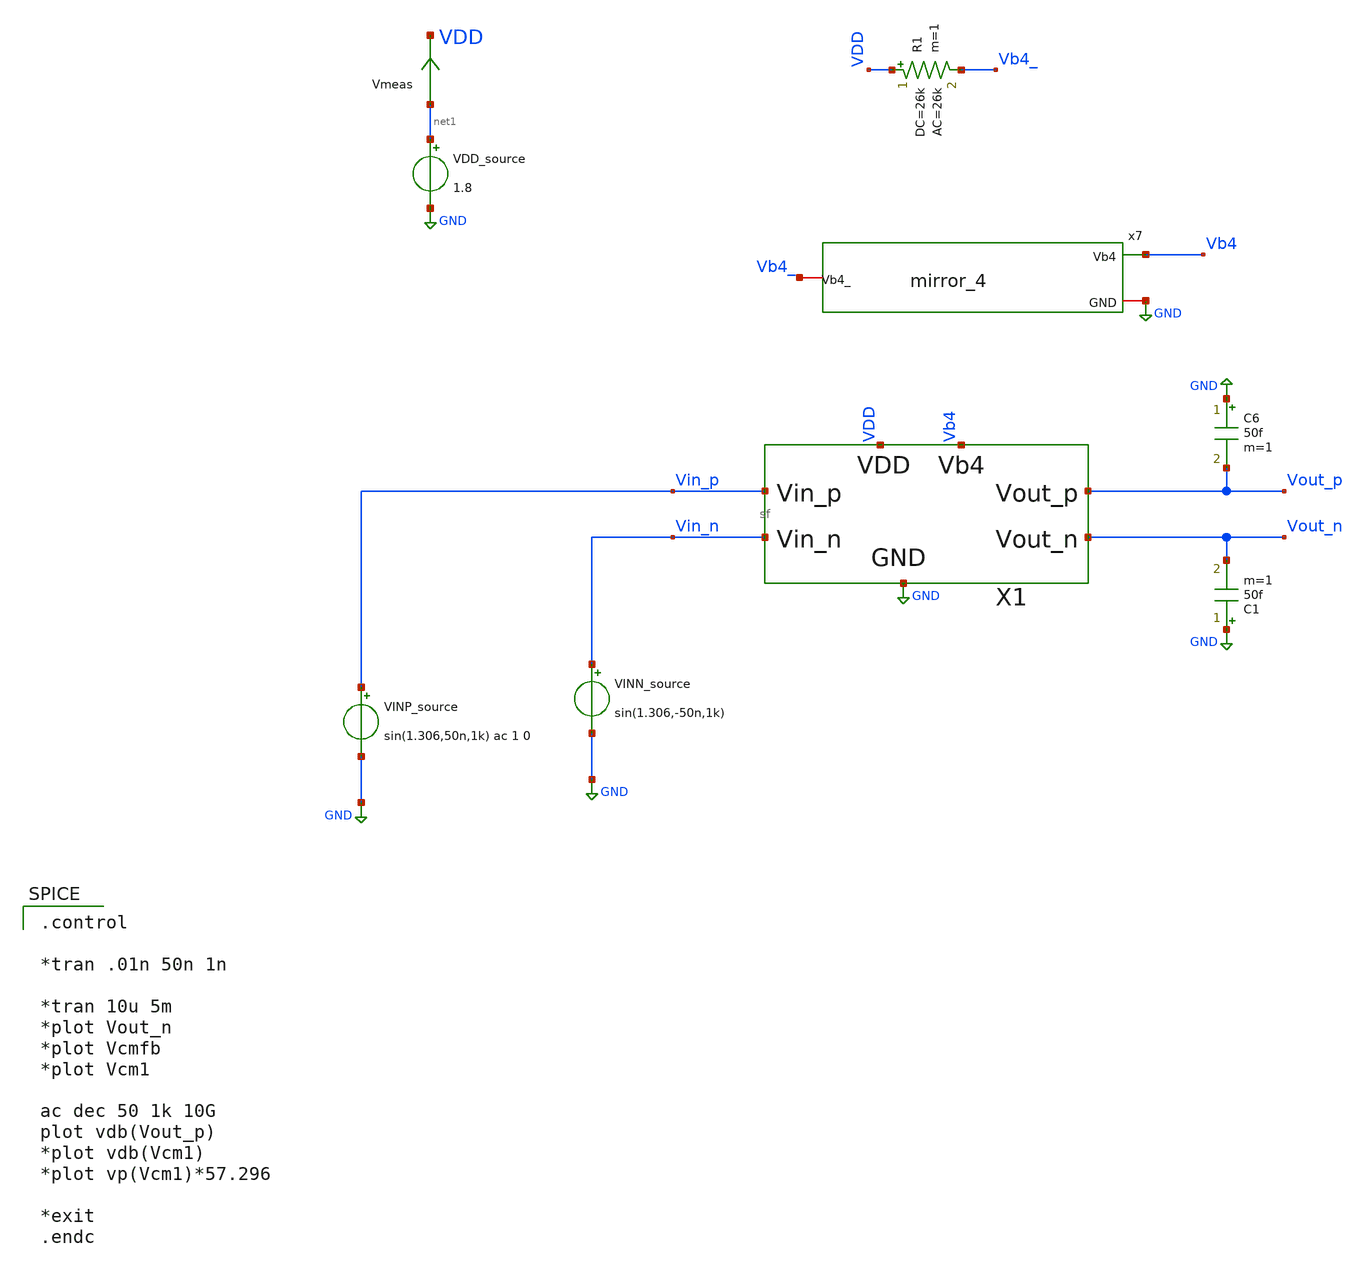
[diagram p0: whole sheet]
** sch_path: xschem/sf_tb.sch
**.subckt sf_tb
VDD_source net1 GND 1.8
Vmeas net1 VDD 0
.save i(vmeas)
C6 GND Vout_p 50f m=1
C1 GND Vout_n 50f m=1
VINP_source Vin_p GND sin(1.306,50n,1k) ac 1 0
VINN_source Vin_n GND sin(1.306,-50n,1k)
X1 VDD GND Vin_p Vin_n Vout_p Vout_n Vb4 sf
R1 VDD Vb4_ 26k ac=26k m=1
x7 Vb4 Vb4_ GND mirror_4
**** begin user architecture code

.include $::SKYWATER_MODELS/cells/nfet_01v8/sky130_fd_pr__nfet_01v8__tt.corner.spice
.include $::SKYWATER_MODELS/cells/pfet_01v8/sky130_fd_pr__pfet_01v8__tt.corner.spice
.include $::SKYWATER_MODELS/cells/nfet_01v8_lvt/sky130_fd_pr__nfet_01v8_lvt__tt.corner.spice
*.include $::SKYWATER_MODELS/cells/nfet_03v3_nvt/sky130_fd_pr__nfet_03v3_nvt__tt.corner.spice
*.include $::SKYWATER_MODELS/cells/nfet_05v0_nvt/sky130_fd_pr__nfet_05v0_nvt__tt.corner.spice
*.include $::SKYWATER_MODELS/cells/esd_nfet_01v8/sky130_fd_pr__esd_nfet_01v8__tt.corner.spice
*.include $::SKYWATER_MODELS/cells/pfet_01v8_lvt/sky130_fd_pr__pfet_01v8_lvt__tt.corner.spice
*.include $::SKYWATER_MODELS/cells/pfet_01v8_hvt/sky130_fd_pr__pfet_01v8_hvt__tt.corner.spice
*.include $::SKYWATER_MODELS/models/corners/tt/nonfet.spice
* Mismatch parameters
.include $::SKYWATER_MODELS/cells/nfet_01v8/sky130_fd_pr__nfet_01v8__mismatch.corner.spice
.include $::SKYWATER_MODELS/cells/pfet_01v8/sky130_fd_pr__pfet_01v8__mismatch.corner.spice
.include $::SKYWATER_MODELS/cells/nfet_01v8_lvt/sky130_fd_pr__nfet_01v8_lvt__mismatch.corner.spice
*.include $::SKYWATER_MODELS/cells/pfet_01v8_lvt/sky130_fd_pr__pfet_01v8_lvt__mismatch.corner.spice
*.include $::SKYWATER_MODELS/cells/pfet_01v8_hvt/sky130_fd_pr__pfet_01v8_hvt__mismatch.corner.spice
*.include $::SKYWATER_MODELS/cells/nfet_g5v0d10v5/sky130_fd_pr__nfet_g5v0d10v5__mismatch.corner.spice
*.include $::SKYWATER_MODELS/cells/pfet_g5v0d10v5/sky130_fd_pr__pfet_g5v0d10v5__mismatch.corner.spice
*.include $::SKYWATER_MODELS/cells/nfet_05v0_nvt/sky130_fd_pr__nfet_05v0_nvt__mismatch.corner.spice
*.include $::SKYWATER_MODELS/cells/nfet_03v3_nvt/sky130_fd_pr__nfet_03v3_nvt__mismatch.corner.spice
* Resistor$::SKYWATER_MODELS/Capacitor
.include $::SKYWATER_MODELS/models/r+c/res_typical__cap_typical.spice
.include $::SKYWATER_MODELS/models/r+c/res_typical__cap_typical__lin.spice
* Special cells
*.include $::SKYWATER_MODELS/models/corners/tt/specialized_cells.spice
* All models
.include $::SKYWATER_MODELS/models/all.spice
* Corner
*.include $::SKYWATER_MODELS/models/corners/tt/rf.spice
.include /home/jared/Documents/GS_Design/tia_post_approval/pex/sf_pex_fixed.spice


.option savecurrents
.control
save all
*NFET

save @m.xm90.msky130_fd_pr__nfet_01v8[vds] @m.xm90.msky130_fd_pr__nfet_01v8[gm]
+ @m.xm90.msky130_fd_pr__nfet_01v8[vth] @m.xm90.msky130_fd_pr__nfet_01v8[vgs] @m.xm90.msky130_fd_pr__nfet_01v8[id]
+ @m.xm90.msky130_fd_pr__nfet_01v8[gds] @m.xm90.msky130_fd_pr__nfet_01v8[cgg] @m.xm90.msky130_fd_pr__nfet_01v8[cgs]
+ @m.xm90.msky130_fd_pr__nfet_01v8[cgd] @m.xm90.msky130_fd_pr__nfet_01v8[cgb] @m.xm90.msky130_fd_pr__nfet_01v8[cdg]
+ @m.xm90.msky130_fd_pr__nfet_01v8[cds] @m.xm90.msky130_fd_pr__nfet_01v8[cdd] @m.xm90.msky130_fd_pr__nfet_01v8[cdb]
+ @m.xm90.msky130_fd_pr__nfet_01v8[csg] @m.xm90.msky130_fd_pr__nfet_01v8[css] @m.xm90.msky130_fd_pr__nfet_01v8[csd]
+ @m.xm90.msky130_fd_pr__nfet_01v8[csb] @m.xm90.msky130_fd_pr__nfet_01v8[cbg] @m.xm90.msky130_fd_pr__nfet_01v8[cbs]
+ @m.xm90.msky130_fd_pr__nfet_01v8[cbd] @m.xm90.msky130_fd_pr__nfet_01v8[cbb]
save @m.xm1.msky130_fd_pr__nfet_01v8[vds] @m.xm1.msky130_fd_pr__nfet_01v8[gm]
+ @m.xm1.msky130_fd_pr__nfet_01v8[vth] @m.xm1.msky130_fd_pr__nfet_01v8[vgs] @m.xm1.msky130_fd_pr__nfet_01v8[id]
+ @m.xm1.msky130_fd_pr__nfet_01v8[gds] @m.xm1.msky130_fd_pr__nfet_01v8[cgg] @m.xm1.msky130_fd_pr__nfet_01v8[cgs]
+ @m.xm1.msky130_fd_pr__nfet_01v8[cgd] @m.xm1.msky130_fd_pr__nfet_01v8[cgb] @m.xm1.msky130_fd_pr__nfet_01v8[cdg]
+ @m.xm1.msky130_fd_pr__nfet_01v8[cds] @m.xm1.msky130_fd_pr__nfet_01v8[cdd] @m.xm1.msky130_fd_pr__nfet_01v8[cdb]
+ @m.xm1.msky130_fd_pr__nfet_01v8[csg] @m.xm1.msky130_fd_pr__nfet_01v8[css] @m.xm1.msky130_fd_pr__nfet_01v8[csd]
+ @m.xm1.msky130_fd_pr__nfet_01v8[csb] @m.xm1.msky130_fd_pr__nfet_01v8[cbg] @m.xm1.msky130_fd_pr__nfet_01v8[cbs]
+ @m.xm1.msky130_fd_pr__nfet_01v8[cbd] @m.xm1.msky130_fd_pr__nfet_01v8[cbb]
save @m.xm2.msky130_fd_pr__nfet_01v8[vds] @m.xm2.msky130_fd_pr__nfet_01v8[gm]
+ @m.xm2.msky130_fd_pr__nfet_01v8[vth] @m.xm2.msky130_fd_pr__nfet_01v8[vgs] @m.xm2.msky130_fd_pr__nfet_01v8[id]
+ @m.xm2.msky130_fd_pr__nfet_01v8[gds] @m.xm2.msky130_fd_pr__nfet_01v8[cgg] @m.xm2.msky130_fd_pr__nfet_01v8[cgs]
+ @m.xm2.msky130_fd_pr__nfet_01v8[cgd] @m.xm2.msky130_fd_pr__nfet_01v8[cgb] @m.xm2.msky130_fd_pr__nfet_01v8[cdg]
+ @m.xm2.msky130_fd_pr__nfet_01v8[cds] @m.xm2.msky130_fd_pr__nfet_01v8[cdd] @m.xm2.msky130_fd_pr__nfet_01v8[cdb]
+ @m.xm2.msky130_fd_pr__nfet_01v8[csg] @m.xm2.msky130_fd_pr__nfet_01v8[css] @m.xm2.msky130_fd_pr__nfet_01v8[csd]
+ @m.xm2.msky130_fd_pr__nfet_01v8[csb] @m.xm2.msky130_fd_pr__nfet_01v8[cbg] @m.xm2.msky130_fd_pr__nfet_01v8[cbs]
+ @m.xm2.msky130_fd_pr__nfet_01v8[cbd] @m.xm2.msky130_fd_pr__nfet_01v8[cbb]
save @m.xm3.msky130_fd_pr__nfet_01v8[vds] @m.xm3.msky130_fd_pr__nfet_01v8[gm]
+ @m.xm3.msky130_fd_pr__nfet_01v8[vth] @m.xm3.msky130_fd_pr__nfet_01v8[vgs] @m.xm3.msky130_fd_pr__nfet_01v8[id]
+ @m.xm3.msky130_fd_pr__nfet_01v8[gds] @m.xm3.msky130_fd_pr__nfet_01v8[cgg] @m.xm3.msky130_fd_pr__nfet_01v8[cgs]
+ @m.xm3.msky130_fd_pr__nfet_01v8[cgd] @m.xm3.msky130_fd_pr__nfet_01v8[cgb] @m.xm3.msky130_fd_pr__nfet_01v8[cdg]
+ @m.xm3.msky130_fd_pr__nfet_01v8[cds] @m.xm3.msky130_fd_pr__nfet_01v8[cdd] @m.xm3.msky130_fd_pr__nfet_01v8[cdb]
+ @m.xm3.msky130_fd_pr__nfet_01v8[csg] @m.xm3.msky130_fd_pr__nfet_01v8[css] @m.xm3.msky130_fd_pr__nfet_01v8[csd]
+ @m.xm3.msky130_fd_pr__nfet_01v8[csb] @m.xm3.msky130_fd_pr__nfet_01v8[cbg] @m.xm3.msky130_fd_pr__nfet_01v8[cbs]
+ @m.xm3.msky130_fd_pr__nfet_01v8[cbd] @m.xm3.msky130_fd_pr__nfet_01v8[cbb]
save @m.xm6.msky130_fd_pr__nfet_01v8[vds] @m.xm6.msky130_fd_pr__nfet_01v8[gm]
+ @m.xm6.msky130_fd_pr__nfet_01v8[vth] @m.xm6.msky130_fd_pr__nfet_01v8[vgs] @m.xm6.msky130_fd_pr__nfet_01v8[id]
+ @m.xm6.msky130_fd_pr__nfet_01v8[gds] @m.xm6.msky130_fd_pr__nfet_01v8[cgg] @m.xm6.msky130_fd_pr__nfet_01v8[cgs]
+ @m.xm6.msky130_fd_pr__nfet_01v8[cgd] @m.xm6.msky130_fd_pr__nfet_01v8[cgb] @m.xm6.msky130_fd_pr__nfet_01v8[cdg]
+ @m.xm6.msky130_fd_pr__nfet_01v8[cds] @m.xm6.msky130_fd_pr__nfet_01v8[cdd] @m.xm6.msky130_fd_pr__nfet_01v8[cdb]
+ @m.xm6.msky130_fd_pr__nfet_01v8[csg] @m.xm6.msky130_fd_pr__nfet_01v8[css] @m.xm6.msky130_fd_pr__nfet_01v8[csd]
+ @m.xm6.msky130_fd_pr__nfet_01v8[csb] @m.xm6.msky130_fd_pr__nfet_01v8[cbg] @m.xm6.msky130_fd_pr__nfet_01v8[cbs]
+ @m.xm6.msky130_fd_pr__nfet_01v8[cbd] @m.xm6.msky130_fd_pr__nfet_01v8[cbb]
save @m.xm7.msky130_fd_pr__nfet_01v8[vds] @m.xm7.msky130_fd_pr__nfet_01v8[gm]
+ @m.xm7.msky130_fd_pr__nfet_01v8[vth] @m.xm7.msky130_fd_pr__nfet_01v8[vgs] @m.xm7.msky130_fd_pr__nfet_01v8[id]
+ @m.xm7.msky130_fd_pr__nfet_01v8[gds] @m.xm7.msky130_fd_pr__nfet_01v8[cgg] @m.xm7.msky130_fd_pr__nfet_01v8[cgs]
+ @m.xm7.msky130_fd_pr__nfet_01v8[cgd] @m.xm7.msky130_fd_pr__nfet_01v8[cgb] @m.xm7.msky130_fd_pr__nfet_01v8[cdg]
+ @m.xm7.msky130_fd_pr__nfet_01v8[cds] @m.xm7.msky130_fd_pr__nfet_01v8[cdd] @m.xm7.msky130_fd_pr__nfet_01v8[cdb]
+ @m.xm7.msky130_fd_pr__nfet_01v8[csg] @m.xm7.msky130_fd_pr__nfet_01v8[css] @m.xm7.msky130_fd_pr__nfet_01v8[csd]
+ @m.xm7.msky130_fd_pr__nfet_01v8[csb] @m.xm7.msky130_fd_pr__nfet_01v8[cbg] @m.xm7.msky130_fd_pr__nfet_01v8[cbs]
+ @m.xm7.msky130_fd_pr__nfet_01v8[cbd] @m.xm7.msky130_fd_pr__nfet_01v8[cbb]
save @m.xm8.msky130_fd_pr__nfet_01v8[vds] @m.xm8.msky130_fd_pr__nfet_01v8[gm]
+ @m.xm8.msky130_fd_pr__nfet_01v8[vth] @m.xm8.msky130_fd_pr__nfet_01v8[vgs] @m.xm8.msky130_fd_pr__nfet_01v8[id]
+ @m.xm8.msky130_fd_pr__nfet_01v8[gds] @m.xm8.msky130_fd_pr__nfet_01v8[cgg] @m.xm8.msky130_fd_pr__nfet_01v8[cgs]
+ @m.xm8.msky130_fd_pr__nfet_01v8[cgd] @m.xm8.msky130_fd_pr__nfet_01v8[cgb] @m.xm8.msky130_fd_pr__nfet_01v8[cdg]
+ @m.xm8.msky130_fd_pr__nfet_01v8[cds] @m.xm8.msky130_fd_pr__nfet_01v8[cdd] @m.xm8.msky130_fd_pr__nfet_01v8[cdb]
+ @m.xm8.msky130_fd_pr__nfet_01v8[csg] @m.xm8.msky130_fd_pr__nfet_01v8[css] @m.xm8.msky130_fd_pr__nfet_01v8[csd]
+ @m.xm8.msky130_fd_pr__nfet_01v8[csb] @m.xm8.msky130_fd_pr__nfet_01v8[cbg] @m.xm8.msky130_fd_pr__nfet_01v8[cbs]
+ @m.xm8.msky130_fd_pr__nfet_01v8[cbd] @m.xm8.msky130_fd_pr__nfet_01v8[cbb]
save @m.xm11.msky130_fd_pr__nfet_01v8[vds] @m.xm11.msky130_fd_pr__nfet_01v8[gm]
+ @m.xm11.msky130_fd_pr__nfet_01v8[vth] @m.xm11.msky130_fd_pr__nfet_01v8[vgs] @m.xm11.msky130_fd_pr__nfet_01v8[id]
+ @m.xm11.msky130_fd_pr__nfet_01v8[gds] @m.xm11.msky130_fd_pr__nfet_01v8[cgg] @m.xm11.msky130_fd_pr__nfet_01v8[cgs]
+ @m.xm11.msky130_fd_pr__nfet_01v8[cgd] @m.xm11.msky130_fd_pr__nfet_01v8[cgb] @m.xm11.msky130_fd_pr__nfet_01v8[cdg]
+ @m.xm11.msky130_fd_pr__nfet_01v8[cds] @m.xm11.msky130_fd_pr__nfet_01v8[cdd] @m.xm11.msky130_fd_pr__nfet_01v8[cdb]
+ @m.xm11.msky130_fd_pr__nfet_01v8[csg] @m.xm11.msky130_fd_pr__nfet_01v8[css] @m.xm11.msky130_fd_pr__nfet_01v8[csd]
+ @m.xm11.msky130_fd_pr__nfet_01v8[csb] @m.xm11.msky130_fd_pr__nfet_01v8[cbg] @m.xm11.msky130_fd_pr__nfet_01v8[cbs]
+ @m.xm11.msky130_fd_pr__nfet_01v8[cbd] @m.xm11.msky130_fd_pr__nfet_01v8[cbb]
save @m.xm12.msky130_fd_pr__nfet_01v8[vds] @m.xm12.msky130_fd_pr__nfet_01v8[gm]
+ @m.xm12.msky130_fd_pr__nfet_01v8[vth] @m.xm12.msky130_fd_pr__nfet_01v8[vgs] @m.xm12.msky130_fd_pr__nfet_01v8[id]
+ @m.xm12.msky130_fd_pr__nfet_01v8[gds] @m.xm12.msky130_fd_pr__nfet_01v8[cgg] @m.xm12.msky130_fd_pr__nfet_01v8[cgs]
+ @m.xm12.msky130_fd_pr__nfet_01v8[cgd] @m.xm12.msky130_fd_pr__nfet_01v8[cgb] @m.xm12.msky130_fd_pr__nfet_01v8[cdg]
+ @m.xm12.msky130_fd_pr__nfet_01v8[cds] @m.xm12.msky130_fd_pr__nfet_01v8[cdd] @m.xm12.msky130_fd_pr__nfet_01v8[cdb]
+ @m.xm12.msky130_fd_pr__nfet_01v8[csg] @m.xm12.msky130_fd_pr__nfet_01v8[css] @m.xm12.msky130_fd_pr__nfet_01v8[csd]
+ @m.xm12.msky130_fd_pr__nfet_01v8[csb] @m.xm12.msky130_fd_pr__nfet_01v8[cbg] @m.xm12.msky130_fd_pr__nfet_01v8[cbs]
+ @m.xm12.msky130_fd_pr__nfet_01v8[cbd] @m.xm12.msky130_fd_pr__nfet_01v8[cbb]
save @m.xm16.msky130_fd_pr__nfet_01v8[vds] @m.xm16.msky130_fd_pr__nfet_01v8[gm]
+ @m.xm16.msky130_fd_pr__nfet_01v8[vth] @m.xm16.msky130_fd_pr__nfet_01v8[vgs] @m.xm16.msky130_fd_pr__nfet_01v8[id]
+ @m.xm16.msky130_fd_pr__nfet_01v8[gds] @m.xm16.msky130_fd_pr__nfet_01v8[cgg] @m.xm16.msky130_fd_pr__nfet_01v8[cgs]
+ @m.xm16.msky130_fd_pr__nfet_01v8[cgd] @m.xm16.msky130_fd_pr__nfet_01v8[cgb] @m.xm16.msky130_fd_pr__nfet_01v8[cdg]
+ @m.xm16.msky130_fd_pr__nfet_01v8[cds] @m.xm16.msky130_fd_pr__nfet_01v8[cdd] @m.xm16.msky130_fd_pr__nfet_01v8[cdb]
+ @m.xm16.msky130_fd_pr__nfet_01v8[csg] @m.xm16.msky130_fd_pr__nfet_01v8[css] @m.xm16.msky130_fd_pr__nfet_01v8[csd]
+ @m.xm16.msky130_fd_pr__nfet_01v8[csb] @m.xm16.msky130_fd_pr__nfet_01v8[cbg] @m.xm16.msky130_fd_pr__nfet_01v8[cbs]
+ @m.xm16.msky130_fd_pr__nfet_01v8[cbd] @m.xm16.msky130_fd_pr__nfet_01v8[cbb]
save @m.xm17.msky130_fd_pr__nfet_01v8_lvt[vds] @m.xm17.msky130_fd_pr__nfet_01v8_lvt[gm]
+ @m.xm17.msky130_fd_pr__nfet_01v8_lvt[vth] @m.xm17.msky130_fd_pr__nfet_01v8_lvt[vgs] @m.xm17.msky130_fd_pr__nfet_01v8_lvt[id]
+ @m.xm17.msky130_fd_pr__nfet_01v8_lvt[gds] @m.xm17.msky130_fd_pr__nfet_01v8_lvt[cgg] @m.xm17.msky130_fd_pr__nfet_01v8_lvt[cgs]
+ @m.xm17.msky130_fd_pr__nfet_01v8_lvt[cgd] @m.xm17.msky130_fd_pr__nfet_01v8_lvt[cgb] @m.xm17.msky130_fd_pr__nfet_01v8_lvt[cdg]
+ @m.xm17.msky130_fd_pr__nfet_01v8_lvt[cds] @m.xm17.msky130_fd_pr__nfet_01v8_lvt[cdd] @m.xm17.msky130_fd_pr__nfet_01v8_lvt[cdb]
+ @m.xm17.msky130_fd_pr__nfet_01v8_lvt[csg] @m.xm17.msky130_fd_pr__nfet_01v8_lvt[css] @m.xm17.msky130_fd_pr__nfet_01v8_lvt[csd]
+ @m.xm17.msky130_fd_pr__nfet_01v8_lvt[csb] @m.xm17.msky130_fd_pr__nfet_01v8_lvt[cbg] @m.xm17.msky130_fd_pr__nfet_01v8_lvt[cbs]
+ @m.xm17.msky130_fd_pr__nfet_01v8_lvt[cbd] @m.xm17.msky130_fd_pr__nfet_01v8_lvt[cbb]
save @m.xm18.msky130_fd_pr__nfet_01v8_lvt[vds] @m.xm18.msky130_fd_pr__nfet_01v8_lvt[gm]
+ @m.xm18.msky130_fd_pr__nfet_01v8_lvt[vth] @m.xm18.msky130_fd_pr__nfet_01v8_lvt[vgs] @m.xm18.msky130_fd_pr__nfet_01v8_lvt[id]
+ @m.xm18.msky130_fd_pr__nfet_01v8_lvt[gds] @m.xm18.msky130_fd_pr__nfet_01v8_lvt[cgg] @m.xm18.msky130_fd_pr__nfet_01v8_lvt[cgs]
+ @m.xm18.msky130_fd_pr__nfet_01v8_lvt[cgd] @m.xm18.msky130_fd_pr__nfet_01v8_lvt[cgb] @m.xm18.msky130_fd_pr__nfet_01v8_lvt[cdg]
+ @m.xm18.msky130_fd_pr__nfet_01v8_lvt[cds] @m.xm18.msky130_fd_pr__nfet_01v8_lvt[cdd] @m.xm18.msky130_fd_pr__nfet_01v8_lvt[cdb]
+ @m.xm18.msky130_fd_pr__nfet_01v8_lvt[csg] @m.xm18.msky130_fd_pr__nfet_01v8_lvt[css] @m.xm18.msky130_fd_pr__nfet_01v8_lvt[csd]
+ @m.xm18.msky130_fd_pr__nfet_01v8_lvt[csb] @m.xm18.msky130_fd_pr__nfet_01v8_lvt[cbg] @m.xm18.msky130_fd_pr__nfet_01v8_lvt[cbs]
+ @m.xm18.msky130_fd_pr__nfet_01v8_lvt[cbd] @m.xm18.msky130_fd_pr__nfet_01v8_lvt[cbb]
save @m.xm19.msky130_fd_pr__nfet_01v8[vds] @m.xm19.msky130_fd_pr__nfet_01v8[gm]
+ @m.xm19.msky130_fd_pr__nfet_01v8[vth] @m.xm19.msky130_fd_pr__nfet_01v8[vgs] @m.xm19.msky130_fd_pr__nfet_01v8[id]
+ @m.xm19.msky130_fd_pr__nfet_01v8[gds] @m.xm19.msky130_fd_pr__nfet_01v8[cgg] @m.xm19.msky130_fd_pr__nfet_01v8[cgs]
+ @m.xm19.msky130_fd_pr__nfet_01v8[cgd] @m.xm19.msky130_fd_pr__nfet_01v8[cgb] @m.xm19.msky130_fd_pr__nfet_01v8[cdg]
+ @m.xm19.msky130_fd_pr__nfet_01v8[cds] @m.xm19.msky130_fd_pr__nfet_01v8[cdd] @m.xm19.msky130_fd_pr__nfet_01v8[cdb]
+ @m.xm19.msky130_fd_pr__nfet_01v8[csg] @m.xm19.msky130_fd_pr__nfet_01v8[css] @m.xm19.msky130_fd_pr__nfet_01v8[csd]
+ @m.xm19.msky130_fd_pr__nfet_01v8[csb] @m.xm19.msky130_fd_pr__nfet_01v8[cbg] @m.xm19.msky130_fd_pr__nfet_01v8[cbs]
+ @m.xm19.msky130_fd_pr__nfet_01v8[cbd] @m.xm19.msky130_fd_pr__nfet_01v8[cbb]
save @m.xm30.msky130_fd_pr__nfet_01v8[vds] @m.xm30.msky130_fd_pr__nfet_01v8[gm]
+ @m.xm30.msky130_fd_pr__nfet_01v8[vth] @m.xm30.msky130_fd_pr__nfet_01v8[vgs] @m.xm30.msky130_fd_pr__nfet_01v8[id]
+ @m.xm30.msky130_fd_pr__nfet_01v8[gds] @m.xm30.msky130_fd_pr__nfet_01v8[cgg] @m.xm30.msky130_fd_pr__nfet_01v8[cgs]
+ @m.xm30.msky130_fd_pr__nfet_01v8[cgd] @m.xm30.msky130_fd_pr__nfet_01v8[cgb] @m.xm30.msky130_fd_pr__nfet_01v8[cdg]
+ @m.xm30.msky130_fd_pr__nfet_01v8[cds] @m.xm30.msky130_fd_pr__nfet_01v8[cdd] @m.xm30.msky130_fd_pr__nfet_01v8[cdb]
+ @m.xm30.msky130_fd_pr__nfet_01v8[csg] @m.xm30.msky130_fd_pr__nfet_01v8[css] @m.xm30.msky130_fd_pr__nfet_01v8[csd]
+ @m.xm30.msky130_fd_pr__nfet_01v8[csb] @m.xm30.msky130_fd_pr__nfet_01v8[cbg] @m.xm30.msky130_fd_pr__nfet_01v8[cbs]
+ @m.xm30.msky130_fd_pr__nfet_01v8[cbd] @m.xm30.msky130_fd_pr__nfet_01v8[cbb]
save @m.xm26.msky130_fd_pr__nfet_01v8[vds] @m.xm26.msky130_fd_pr__nfet_01v8[gm]
+ @m.xm26.msky130_fd_pr__nfet_01v8[vth] @m.xm26.msky130_fd_pr__nfet_01v8[vgs] @m.xm26.msky130_fd_pr__nfet_01v8[id]
+ @m.xm26.msky130_fd_pr__nfet_01v8[gds] @m.xm26.msky130_fd_pr__nfet_01v8[cgg] @m.xm26.msky130_fd_pr__nfet_01v8[cgs]
+ @m.xm26.msky130_fd_pr__nfet_01v8[cgd] @m.xm26.msky130_fd_pr__nfet_01v8[cgb] @m.xm26.msky130_fd_pr__nfet_01v8[cdg]
+ @m.xm26.msky130_fd_pr__nfet_01v8[cds] @m.xm26.msky130_fd_pr__nfet_01v8[cdd] @m.xm26.msky130_fd_pr__nfet_01v8[cdb]
+ @m.xm26.msky130_fd_pr__nfet_01v8[csg] @m.xm26.msky130_fd_pr__nfet_01v8[css] @m.xm26.msky130_fd_pr__nfet_01v8[csd]
+ @m.xm26.msky130_fd_pr__nfet_01v8[csb] @m.xm26.msky130_fd_pr__nfet_01v8[cbg] @m.xm26.msky130_fd_pr__nfet_01v8[cbs]
+ @m.xm26.msky130_fd_pr__nfet_01v8[cbd] @m.xm26.msky130_fd_pr__nfet_01v8[cbb]
save @m.xm27.msky130_fd_pr__nfet_01v8[vds] @m.xm27.msky130_fd_pr__nfet_01v8[gm]
+ @m.xm27.msky130_fd_pr__nfet_01v8[vth] @m.xm27.msky130_fd_pr__nfet_01v8[vgs] @m.xm27.msky130_fd_pr__nfet_01v8[id]
+ @m.xm27.msky130_fd_pr__nfet_01v8[gds] @m.xm27.msky130_fd_pr__nfet_01v8[cgg] @m.xm27.msky130_fd_pr__nfet_01v8[cgs]
+ @m.xm27.msky130_fd_pr__nfet_01v8[cgd] @m.xm27.msky130_fd_pr__nfet_01v8[cgb] @m.xm27.msky130_fd_pr__nfet_01v8[cdg]
+ @m.xm27.msky130_fd_pr__nfet_01v8[cds] @m.xm27.msky130_fd_pr__nfet_01v8[cdd] @m.xm27.msky130_fd_pr__nfet_01v8[cdb]
+ @m.xm27.msky130_fd_pr__nfet_01v8[csg] @m.xm27.msky130_fd_pr__nfet_01v8[css] @m.xm27.msky130_fd_pr__nfet_01v8[csd]
+ @m.xm27.msky130_fd_pr__nfet_01v8[csb] @m.xm27.msky130_fd_pr__nfet_01v8[cbg] @m.xm27.msky130_fd_pr__nfet_01v8[cbs]
+ @m.xm27.msky130_fd_pr__nfet_01v8[cbd] @m.xm27.msky130_fd_pr__nfet_01v8[cbb]

*PFET

save @m.xm91.msky130_fd_pr__pfet_01v8[vds] @m.xm91.msky130_fd_pr__pfet_01v8[gm]
+ @m.xm91.msky130_fd_pr__pfet_01v8[vth] @m.xm91.msky130_fd_pr__pfet_01v8[vgs] @m.xm91.msky130_fd_pr__pfet_01v8[id]
+ @m.xm91.msky130_fd_pr__pfet_01v8[gds] @m.xm91.msky130_fd_pr__pfet_01v8[cgg] @m.xm91.msky130_fd_pr__pfet_01v8[cgs]
+ @m.xm91.msky130_fd_pr__pfet_01v8[cgd] @m.xm91.msky130_fd_pr__pfet_01v8[cgb] @m.xm91.msky130_fd_pr__pfet_01v8[cdg]
+ @m.xm91.msky130_fd_pr__pfet_01v8[cds] @m.xm91.msky130_fd_pr__pfet_01v8[cdd] @m.xm91.msky130_fd_pr__pfet_01v8[cdb]
+ @m.xm91.msky130_fd_pr__pfet_01v8[csg] @m.xm91.msky130_fd_pr__pfet_01v8[css] @m.xm91.msky130_fd_pr__pfet_01v8[csd]
+ @m.xm91.msky130_fd_pr__pfet_01v8[csb] @m.xm91.msky130_fd_pr__pfet_01v8[cbg] @m.xm91.msky130_fd_pr__pfet_01v8[cbs]
+ @m.xm91.msky130_fd_pr__pfet_01v8[cbd] @m.xm91.msky130_fd_pr__pfet_01v8[cbb]
save @m.xm4.msky130_fd_pr__pfet_01v8[vds] @m.xm4.msky130_fd_pr__pfet_01v8[gm]
+ @m.xm4.msky130_fd_pr__pfet_01v8[vth] @m.xm4.msky130_fd_pr__pfet_01v8[vgs] @m.xm4.msky130_fd_pr__pfet_01v8[id]
+ @m.xm4.msky130_fd_pr__pfet_01v8[gds] @m.xm4.msky130_fd_pr__pfet_01v8[cgg] @m.xm4.msky130_fd_pr__pfet_01v8[cgs]
+ @m.xm4.msky130_fd_pr__pfet_01v8[cgd] @m.xm4.msky130_fd_pr__pfet_01v8[cgb] @m.xm4.msky130_fd_pr__pfet_01v8[cdg]
+ @m.xm4.msky130_fd_pr__pfet_01v8[cds] @m.xm4.msky130_fd_pr__pfet_01v8[cdd] @m.xm4.msky130_fd_pr__pfet_01v8[cdb]
+ @m.xm4.msky130_fd_pr__pfet_01v8[csg] @m.xm4.msky130_fd_pr__pfet_01v8[css] @m.xm4.msky130_fd_pr__pfet_01v8[csd]
+ @m.xm4.msky130_fd_pr__pfet_01v8[csb] @m.xm4.msky130_fd_pr__pfet_01v8[cbg] @m.xm4.msky130_fd_pr__pfet_01v8[cbs]
+ @m.xm4.msky130_fd_pr__pfet_01v8[cbd] @m.xm4.msky130_fd_pr__pfet_01v8[cbb]
save @m.xm5.msky130_fd_pr__pfet_01v8[vds] @m.xm5.msky130_fd_pr__pfet_01v8[gm]
+ @m.xm5.msky130_fd_pr__pfet_01v8[vth] @m.xm5.msky130_fd_pr__pfet_01v8[vgs] @m.xm5.msky130_fd_pr__pfet_01v8[id]
+ @m.xm5.msky130_fd_pr__pfet_01v8[gds] @m.xm5.msky130_fd_pr__pfet_01v8[cgg] @m.xm5.msky130_fd_pr__pfet_01v8[cgs]
+ @m.xm5.msky130_fd_pr__pfet_01v8[cgd] @m.xm5.msky130_fd_pr__pfet_01v8[cgb] @m.xm5.msky130_fd_pr__pfet_01v8[cdg]
+ @m.xm5.msky130_fd_pr__pfet_01v8[cds] @m.xm5.msky130_fd_pr__pfet_01v8[cdd] @m.xm5.msky130_fd_pr__pfet_01v8[cdb]
+ @m.xm5.msky130_fd_pr__pfet_01v8[csg] @m.xm5.msky130_fd_pr__pfet_01v8[css] @m.xm5.msky130_fd_pr__pfet_01v8[csd]
+ @m.xm5.msky130_fd_pr__pfet_01v8[csb] @m.xm5.msky130_fd_pr__pfet_01v8[cbg] @m.xm5.msky130_fd_pr__pfet_01v8[cbs]
+ @m.xm5.msky130_fd_pr__pfet_01v8[cbd] @m.xm5.msky130_fd_pr__pfet_01v8[cbb]
save @m.xm9.msky130_fd_pr__pfet_01v8[vds] @m.xm9.msky130_fd_pr__pfet_01v8[gm]
+ @m.xm9.msky130_fd_pr__pfet_01v8[vth] @m.xm9.msky130_fd_pr__pfet_01v8[vgs] @m.xm9.msky130_fd_pr__pfet_01v8[id]
+ @m.xm9.msky130_fd_pr__pfet_01v8[gds] @m.xm9.msky130_fd_pr__pfet_01v8[cgg] @m.xm9.msky130_fd_pr__pfet_01v8[cgs]
+ @m.xm9.msky130_fd_pr__pfet_01v8[cgd] @m.xm9.msky130_fd_pr__pfet_01v8[cgb] @m.xm9.msky130_fd_pr__pfet_01v8[cdg]
+ @m.xm9.msky130_fd_pr__pfet_01v8[cds] @m.xm9.msky130_fd_pr__pfet_01v8[cdd] @m.xm9.msky130_fd_pr__pfet_01v8[cdb]
+ @m.xm9.msky130_fd_pr__pfet_01v8[csg] @m.xm9.msky130_fd_pr__pfet_01v8[css] @m.xm9.msky130_fd_pr__pfet_01v8[csd]
+ @m.xm9.msky130_fd_pr__pfet_01v8[csb] @m.xm9.msky130_fd_pr__pfet_01v8[cbg] @m.xm9.msky130_fd_pr__pfet_01v8[cbs]
+ @m.xm9.msky130_fd_pr__pfet_01v8[cbd] @m.xm9.msky130_fd_pr__pfet_01v8[cbb]
save @m.xm10.msky130_fd_pr__pfet_01v8[vds] @m.xm10.msky130_fd_pr__pfet_01v8[gm]
+ @m.xm10.msky130_fd_pr__pfet_01v8[vth] @m.xm10.msky130_fd_pr__pfet_01v8[vgs] @m.xm10.msky130_fd_pr__pfet_01v8[id]
+ @m.xm10.msky130_fd_pr__pfet_01v8[gds] @m.xm10.msky130_fd_pr__pfet_01v8[cgg] @m.xm10.msky130_fd_pr__pfet_01v8[cgs]
+ @m.xm10.msky130_fd_pr__pfet_01v8[cgd] @m.xm10.msky130_fd_pr__pfet_01v8[cgb] @m.xm10.msky130_fd_pr__pfet_01v8[cdg]
+ @m.xm10.msky130_fd_pr__pfet_01v8[cds] @m.xm10.msky130_fd_pr__pfet_01v8[cdd] @m.xm10.msky130_fd_pr__pfet_01v8[cdb]
+ @m.xm10.msky130_fd_pr__pfet_01v8[csg] @m.xm10.msky130_fd_pr__pfet_01v8[css] @m.xm10.msky130_fd_pr__pfet_01v8[csd]
+ @m.xm10.msky130_fd_pr__pfet_01v8[csb] @m.xm10.msky130_fd_pr__pfet_01v8[cbg] @m.xm10.msky130_fd_pr__pfet_01v8[cbs]
+ @m.xm10.msky130_fd_pr__pfet_01v8[cbd] @m.xm10.msky130_fd_pr__pfet_01v8[cbb]
save @m.xm13.msky130_fd_pr__pfet_01v8[vds] @m.xm13.msky130_fd_pr__pfet_01v8[gm]
+ @m.xm13.msky130_fd_pr__pfet_01v8[vth] @m.xm13.msky130_fd_pr__pfet_01v8[vgs] @m.xm13.msky130_fd_pr__pfet_01v8[id]
+ @m.xm13.msky130_fd_pr__pfet_01v8[gds] @m.xm13.msky130_fd_pr__pfet_01v8[cgg] @m.xm13.msky130_fd_pr__pfet_01v8[cgs]
+ @m.xm13.msky130_fd_pr__pfet_01v8[cgd] @m.xm13.msky130_fd_pr__pfet_01v8[cgb] @m.xm13.msky130_fd_pr__pfet_01v8[cdg]
+ @m.xm13.msky130_fd_pr__pfet_01v8[cds] @m.xm13.msky130_fd_pr__pfet_01v8[cdd] @m.xm13.msky130_fd_pr__pfet_01v8[cdb]
+ @m.xm13.msky130_fd_pr__pfet_01v8[csg] @m.xm13.msky130_fd_pr__pfet_01v8[css] @m.xm13.msky130_fd_pr__pfet_01v8[csd]
+ @m.xm13.msky130_fd_pr__pfet_01v8[csb] @m.xm13.msky130_fd_pr__pfet_01v8[cbg] @m.xm13.msky130_fd_pr__pfet_01v8[cbs]
+ @m.xm13.msky130_fd_pr__pfet_01v8[cbd] @m.xm13.msky130_fd_pr__pfet_01v8[cbb]
save @m.xm14.msky130_fd_pr__pfet_01v8[vds] @m.xm14.msky130_fd_pr__pfet_01v8[gm]
+ @m.xm14.msky130_fd_pr__pfet_01v8[vth] @m.xm14.msky130_fd_pr__pfet_01v8[vgs] @m.xm14.msky130_fd_pr__pfet_01v8[id]
+ @m.xm14.msky130_fd_pr__pfet_01v8[gds] @m.xm14.msky130_fd_pr__pfet_01v8[cgg] @m.xm14.msky130_fd_pr__pfet_01v8[cgs]
+ @m.xm14.msky130_fd_pr__pfet_01v8[cgd] @m.xm14.msky130_fd_pr__pfet_01v8[cgb] @m.xm14.msky130_fd_pr__pfet_01v8[cdg]
+ @m.xm14.msky130_fd_pr__pfet_01v8[cds] @m.xm14.msky130_fd_pr__pfet_01v8[cdd] @m.xm14.msky130_fd_pr__pfet_01v8[cdb]
+ @m.xm14.msky130_fd_pr__pfet_01v8[csg] @m.xm14.msky130_fd_pr__pfet_01v8[css] @m.xm14.msky130_fd_pr__pfet_01v8[csd]
+ @m.xm14.msky130_fd_pr__pfet_01v8[csb] @m.xm14.msky130_fd_pr__pfet_01v8[cbg] @m.xm14.msky130_fd_pr__pfet_01v8[cbs]
+ @m.xm14.msky130_fd_pr__pfet_01v8[cbd] @m.xm14.msky130_fd_pr__pfet_01v8[cbb]
save @m.xm24.msky130_fd_pr__pfet_01v8[vds] @m.xm24.msky130_fd_pr__pfet_01v8[gm]
+ @m.xm24.msky130_fd_pr__pfet_01v8[vth] @m.xm24.msky130_fd_pr__pfet_01v8[vgs] @m.xm24.msky130_fd_pr__pfet_01v8[id]
+ @m.xm24.msky130_fd_pr__pfet_01v8[gds] @m.xm24.msky130_fd_pr__pfet_01v8[cgg] @m.xm24.msky130_fd_pr__pfet_01v8[cgs]
+ @m.xm24.msky130_fd_pr__pfet_01v8[cgd] @m.xm24.msky130_fd_pr__pfet_01v8[cgb] @m.xm24.msky130_fd_pr__pfet_01v8[cdg]
+ @m.xm24.msky130_fd_pr__pfet_01v8[cds] @m.xm24.msky130_fd_pr__pfet_01v8[cdd] @m.xm24.msky130_fd_pr__pfet_01v8[cdb]
+ @m.xm24.msky130_fd_pr__pfet_01v8[csg] @m.xm24.msky130_fd_pr__pfet_01v8[css] @m.xm24.msky130_fd_pr__pfet_01v8[csd]
+ @m.xm24.msky130_fd_pr__pfet_01v8[csb] @m.xm24.msky130_fd_pr__pfet_01v8[cbg] @m.xm24.msky130_fd_pr__pfet_01v8[cbs]
+ @m.xm24.msky130_fd_pr__pfet_01v8[cbd] @m.xm24.msky130_fd_pr__pfet_01v8[cbb]
save @m.xm25.msky130_fd_pr__pfet_01v8[vds] @m.xm25.msky130_fd_pr__pfet_01v8[gm]
+ @m.xm25.msky130_fd_pr__pfet_01v8[vth] @m.xm25.msky130_fd_pr__pfet_01v8[vgs] @m.xm25.msky130_fd_pr__pfet_01v8[id]
+ @m.xm25.msky130_fd_pr__pfet_01v8[gds] @m.xm25.msky130_fd_pr__pfet_01v8[cgg] @m.xm25.msky130_fd_pr__pfet_01v8[cgs]
+ @m.xm25.msky130_fd_pr__pfet_01v8[cgd] @m.xm25.msky130_fd_pr__pfet_01v8[cgb] @m.xm25.msky130_fd_pr__pfet_01v8[cdg]
+ @m.xm25.msky130_fd_pr__pfet_01v8[cds] @m.xm25.msky130_fd_pr__pfet_01v8[cdd] @m.xm25.msky130_fd_pr__pfet_01v8[cdb]
+ @m.xm25.msky130_fd_pr__pfet_01v8[csg] @m.xm25.msky130_fd_pr__pfet_01v8[css] @m.xm25.msky130_fd_pr__pfet_01v8[csd]
+ @m.xm25.msky130_fd_pr__pfet_01v8[csb] @m.xm25.msky130_fd_pr__pfet_01v8[cbg] @m.xm25.msky130_fd_pr__pfet_01v8[cbs]
+ @m.xm25.msky130_fd_pr__pfet_01v8[cbd] @m.xm25.msky130_fd_pr__pfet_01v8[cbb]

op
write sf_tb.raw
.endc


.control

*tran .01n 50n 1n

*tran 10u 5m
*plot Vout_n
*plot Vcmfb
*plot Vcm1

ac dec 50 1k 10G
plot vdb(Vout_p)
*plot vdb(Vcm1)
*plot vp(Vcm1)*57.296

*exit
.endc


**** end user architecture code
**.ends

* expanding   symbol:  tia_post_approval/schem/sf.sym # of pins=7
** sym_path: xschem/sf.sym
** sch_path: xschem/sf.sch
.subckt sf VDD GND Vin_p Vin_n Vout_p Vout_n Vb4
*.ipin Vin_n
*.iopin VDD
*.iopin GND
*.ipin Vin_p
*.opin Vout_n
*.opin Vout_p
*.iopin Vb4
X1 VDD Vb4 Vout_p Vin_p GND sf_half
X2 VDD Vb4 Vout_n Vin_n GND sf_half
.ends


* expanding   symbol:  tia_post_approval/schem/mirror_4.sym # of pins=3
** sym_path: tia_post_approval/schem/mirror_4.sym
** sch_path: tia_post_approval/schem/mirror_4.sch
.subckt mirror_4 Vb4 Vb4_ GND
*.iopin GND
*.iopin Vb4_
*.opin Vb4
XM27 Vb4_ Vb4_ GND GND sky130_fd_pr__nfet_01v8 L=.45 W=4 nf=1 ad='int((nf+1)/2) * W/nf * 0.29' as='int((nf+2)/2) * W/nf * 0.29'
+ pd='2*int((nf+1)/2) * (W/nf + 0.29)' ps='2*int((nf+2)/2) * (W/nf + 0.29)' nrd='0.29 / W' nrs='0.29 / W'
+ sa=0 sb=0 sd=0 mult=1 m=1
XC1 Vb4 GND sky130_fd_pr__cap_mim_m3_1 W=15.8 L=15.8 MF=1 m=1
XC2 GND Vb4 sky130_fd_pr__cap_mim_m3_2 W=15.8 L=15.8 MF=1 m=1
XR11 V10 Vb4 GND sky130_fd_pr__res_xhigh_po W=0.35 L=16 mult=1 m=1
XR1 Vb4_ V1 GND sky130_fd_pr__res_xhigh_po W=0.35 L=16 mult=1 m=1
XR2 V10 V9 GND sky130_fd_pr__res_xhigh_po W=0.35 L=16 mult=1 m=1
XR3 V2 V1 GND sky130_fd_pr__res_xhigh_po W=0.35 L=16 mult=1 m=1
XR4 V8 V9 GND sky130_fd_pr__res_xhigh_po W=0.35 L=16 mult=1 m=1
XR5 V2 V3 GND sky130_fd_pr__res_xhigh_po W=0.35 L=16 mult=1 m=1
XR6 V8 V7 GND sky130_fd_pr__res_xhigh_po W=0.35 L=16 mult=1 m=1
XR7 V4 V3 GND sky130_fd_pr__res_xhigh_po W=0.35 L=16 mult=1 m=1
XR8 V6 V7 GND sky130_fd_pr__res_xhigh_po W=0.35 L=16 mult=1 m=1
XR9 V4 V5 GND sky130_fd_pr__res_xhigh_po W=0.35 L=16 mult=1 m=1
XR10 V6 V5 GND sky130_fd_pr__res_xhigh_po W=0.35 L=16 mult=1 m=1
XM1 GND GND Vb4_ GND sky130_fd_pr__nfet_01v8 L=.45 W=4 nf=1 ad='int((nf+1)/2) * W/nf * 0.29' as='int((nf+2)/2) * W/nf * 0.29'
+ pd='2*int((nf+1)/2) * (W/nf + 0.29)' ps='2*int((nf+2)/2) * (W/nf + 0.29)' nrd='0.29 / W' nrs='0.29 / W'
+ sa=0 sb=0 sd=0 mult=1 m=1
XM2 GND GND GND GND sky130_fd_pr__nfet_01v8 L=.45 W=4 nf=1 ad='int((nf+1)/2) * W/nf * 0.29' as='int((nf+2)/2) * W/nf * 0.29'
+ pd='2*int((nf+1)/2) * (W/nf + 0.29)' ps='2*int((nf+2)/2) * (W/nf + 0.29)' nrd='0.29 / W' nrs='0.29 / W'
+ sa=0 sb=0 sd=0 mult=1 m=1
.ends


* expanding   symbol:  sscs_pico_chip_4/xschem/sf_half.sym # of pins=5
** sym_path: sscs_pico_chip_4/xschem/sf_half.sym
** sch_path: sscs_pico_chip_4/xschem/sf_half.sch
.subckt sf_half VDD g_d Vout g_u GND
*.iopin VDD
*.iopin g_u
*.iopin GND
*.iopin Vout
*.iopin g_d
XM17 VDD g_u Vout Vout sky130_fd_pr__nfet_01v8_lvt L=0.32 W=650 nf=26 ad='int((nf+1)/2) * W/nf * 0.29'
+ as='int((nf+2)/2) * W/nf * 0.29' pd='2*int((nf+1)/2) * (W/nf + 0.29)' ps='2*int((nf+2)/2) * (W/nf + 0.29)'
+ nrd='0.29 / W' nrs='0.29 / W' sa=0 sb=0 sd=0 mult=1 m=1
XM19 Vout g_d GND GND sky130_fd_pr__nfet_01v8 L=.45 W=650 nf=26 ad='int((nf+1)/2) * W/nf * 0.29' as='int((nf+2)/2) * W/nf * 0.29'
+ pd='2*int((nf+1)/2) * (W/nf + 0.29)' ps='2*int((nf+2)/2) * (W/nf + 0.29)' nrd='0.29 / W' nrs='0.29 / W'
+ sa=0 sb=0 sd=0 mult=1 m=1
.ends

.GLOBAL GND
.end
